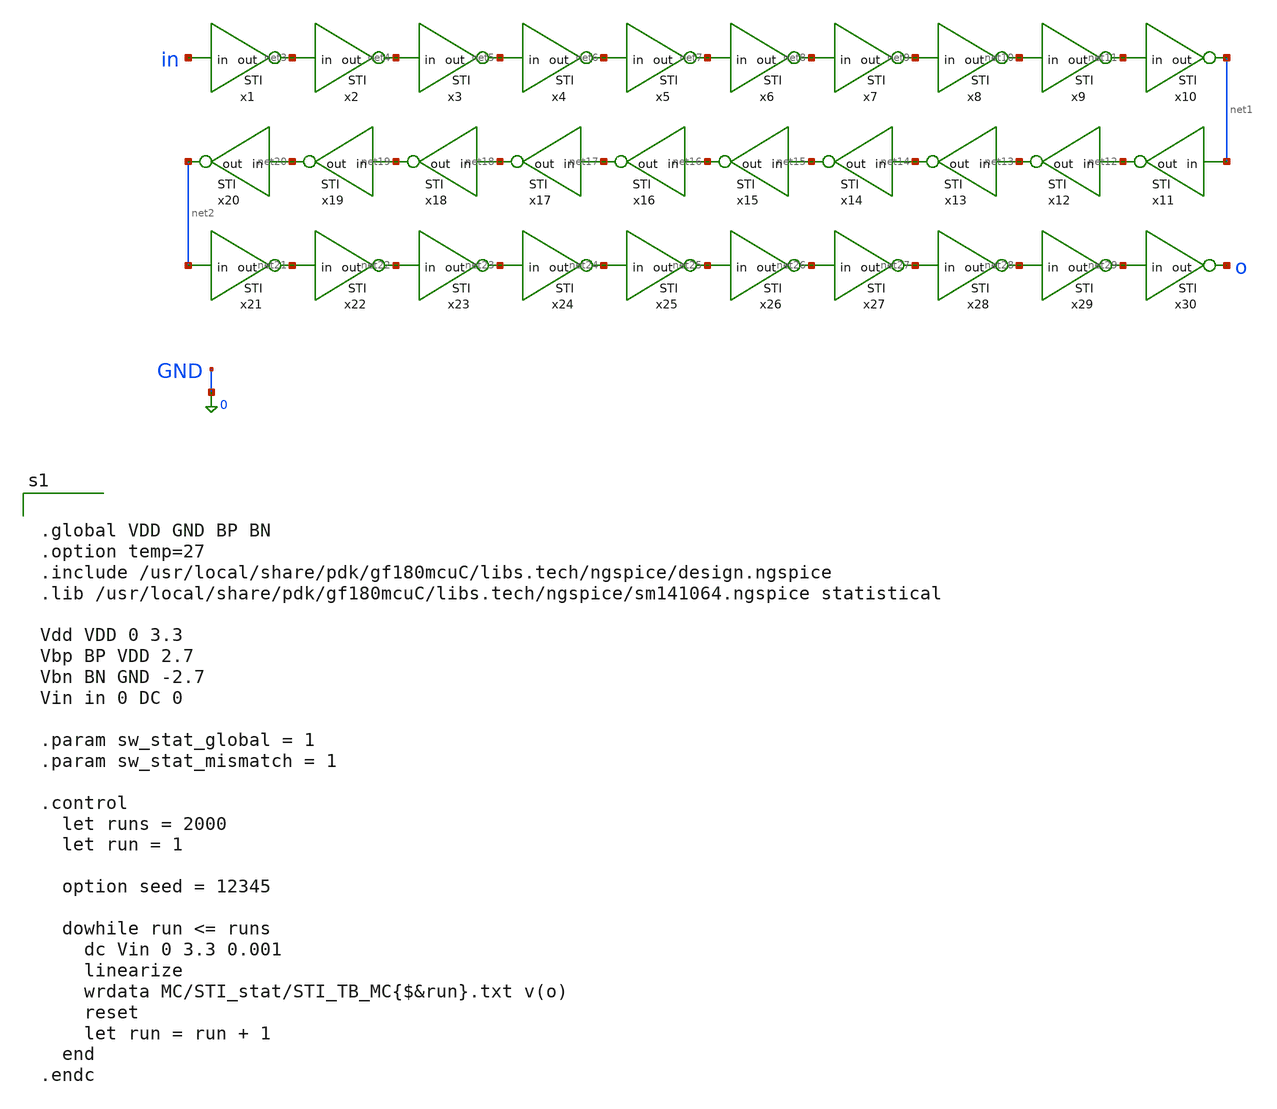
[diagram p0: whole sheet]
** sch_path: xschem_designs/STI_TB_MC.sch
**.subckt STI_TB_MC
x1 in net3 STI
x2 net3 net4 STI
x3 net4 net5 STI
x4 net5 net6 STI
x5 net6 net7 STI
x6 net7 net8 STI
x7 net8 net9 STI
x8 net9 net10 STI
x9 net10 net11 STI
x10 net11 net1 STI
x11 net1 net12 STI
x12 net12 net13 STI
x13 net13 net14 STI
x14 net14 net15 STI
x15 net15 net16 STI
x16 net16 net17 STI
x17 net17 net18 STI
x18 net18 net19 STI
x19 net19 net20 STI
x20 net20 net2 STI
x21 net2 net21 STI
x22 net21 net22 STI
x23 net22 net23 STI
x24 net23 net24 STI
x25 net24 net25 STI
x26 net25 net26 STI
x27 net26 net27 STI
x28 net27 net28 STI
x29 net28 net29 STI
x30 net29 o STI
**** begin user architecture code


.global VDD GND BP BN
.option temp=27
.include /usr/local/share/pdk/gf180mcuC/libs.tech/ngspice/design.ngspice
.lib /usr/local/share/pdk/gf180mcuC/libs.tech/ngspice/sm141064.ngspice statistical

Vdd VDD 0 3.3
Vbp BP VDD 2.7
Vbn BN GND -2.7
Vin in 0 DC 0

.param sw_stat_global = 1
.param sw_stat_mismatch = 1

.control
  let runs = 2000
  let run = 1

  option seed = 12345

  dowhile run <= runs
    dc Vin 0 3.3 0.001
    linearize
    wrdata MC/STI_stat/STI_TB_MC{$&run}.txt v(o)
    reset
    let run = run + 1
  end
.endc


**** end user architecture code
**.ends

* expanding   symbol:  xschem_designs/STI.sym # of pins=2
** sym_path: xschem_designs/STI.sym
** sch_path: xschem_designs/STI.sch
.subckt STI in out
*.ipin in
*.opin out
XM225 out out net1 GND nfet_03v3 L=2.24u W=0.22u nf=1 ad='int((nf+1)/2) * W/nf * 0.18u' as='int((nf+2)/2) * W/nf * 0.18u'
+ pd='2*int((nf+1)/2) * (W/nf + 0.18u)' ps='2*int((nf+2)/2) * (W/nf + 0.18u)' nrd='0.18u / W' nrs='0.18u / W'
+ sa=0 sb=0 sd=0 m=1 par=1
XM226 out out net2 VDD pfet_03v3 L=1.12u W=0.22u nf=1 ad='int((nf+1)/2) * W/nf * 0.18u' as='int((nf+2)/2) * W/nf * 0.18u'
+ pd='2*int((nf+1)/2) * (W/nf + 0.18u)' ps='2*int((nf+2)/2) * (W/nf + 0.18u)' nrd='0.18u / W' nrs='0.18u / W'
+ sa=0 sb=0 sd=0 m=1 par=1
XM237 net2 in VDD VDD pfet_03v3 L=0.28u W=0.44u nf=1 ad='int((nf+1)/2) * W/nf * 0.18u' as='int((nf+2)/2) * W/nf * 0.18u'
+ pd='2*int((nf+1)/2) * (W/nf + 0.18u)' ps='2*int((nf+2)/2) * (W/nf + 0.18u)' nrd='0.18u / W' nrs='0.18u / W'
+ sa=0 sb=0 sd=0 m=1 par=1
XM238 net1 in GND GND nfet_03v3 L=0.28u W=0.22u nf=1 ad='int((nf+1)/2) * W/nf * 0.18u' as='int((nf+2)/2) * W/nf * 0.18u'
+ pd='2*int((nf+1)/2) * (W/nf + 0.18u)' ps='2*int((nf+2)/2) * (W/nf + 0.18u)' nrd='0.18u / W' nrs='0.18u / W'
+ sa=0 sb=0 sd=0 m=1 par=1
XM241 out in VDD BP pfet_06v0 L=1.1u W=0.60u nf=1 ad='int((nf+1)/2) * W/nf * 0.18u' as='int((nf+2)/2) * W/nf * 0.18u'
+ pd='2*int((nf+1)/2) * (W/nf + 0.18u)' ps='2*int((nf+2)/2) * (W/nf + 0.18u)' nrd='0.18u / W' nrs='0.18u / W'
+ sa=0 sb=0 sd=0 m=1 par=1
XM242 out in GND BN nfet_06v0 L=1.4u W=0.30u nf=1 ad='int((nf+1)/2) * W/nf * 0.18u' as='int((nf+2)/2) * W/nf * 0.18u'
+ pd='2*int((nf+1)/2) * (W/nf + 0.18u)' ps='2*int((nf+2)/2) * (W/nf + 0.18u)' nrd='0.18u / W' nrs='0.18u / W'
+ sa=0 sb=0 sd=0 m=1 par=1
.ends

.end
